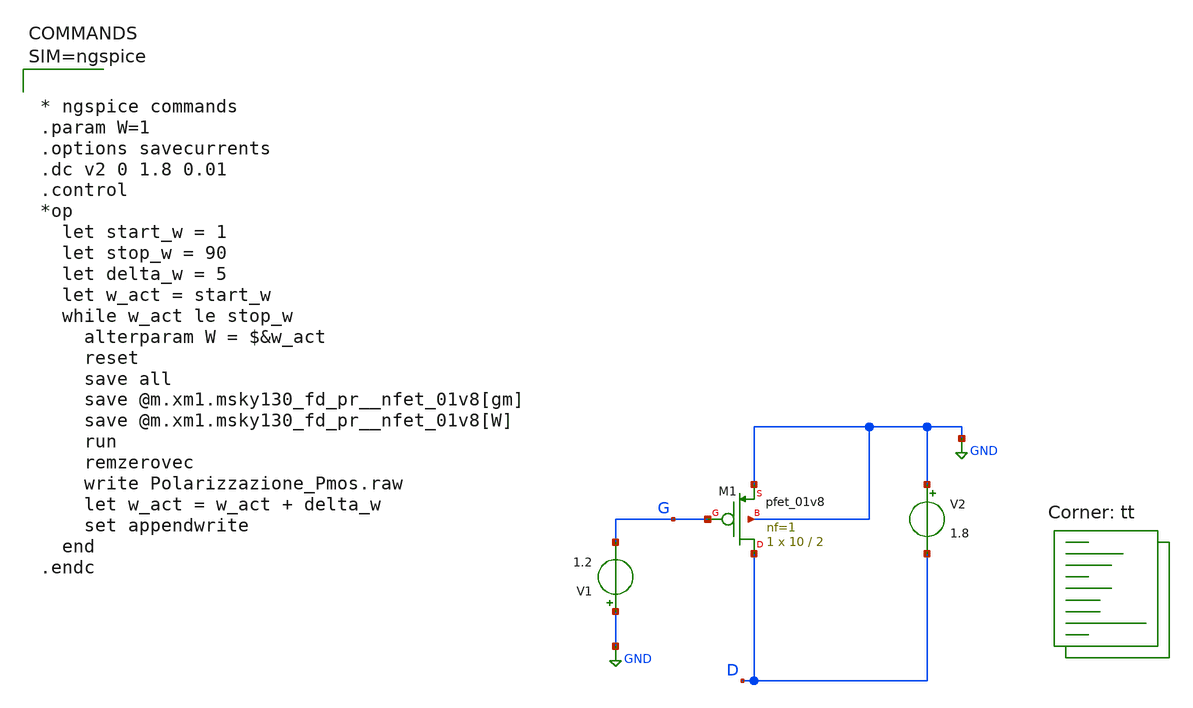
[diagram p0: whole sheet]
** sch_path: xschem/Polarizzazione_Pmos.sch
* Copyright 2021 Stefan Frederik Schippers
* Licensed under the Apache License, Version 2.0 (the "License");
* you may not use this file except in compliance with the License.
* You may obtain a copy of the License at
* https://www.apache.org/licenses/LICENSE-2.0
* Unless required by applicable law or agreed to in writing, software
* distributed under the License is distributed on an "AS IS" BASIS,
* WITHOUT WARRANTIES OR CONDITIONS OF ANY KIND, either express or implied.
* See the License for the specific language governing permissions and
* limitations under the License.
**.subckt Polarizzazione_Pmos
V1 GND G 1.2
V2 GND D 1.8
XM1 D G GND GND sky130_fd_pr__pfet_01v8 L=2 W=10 nf=1 ad='int((nf+1)/2) * W/nf * 0.29' as='int((nf+2)/2) * W/nf * 0.29'
+ pd='2*int((nf+1)/2) * (W/nf + 0.29)' ps='2*int((nf+2)/2) * (W/nf + 0.29)' nrd='0.29 / W' nrs='0.29 / W'
+ sa=0 sb=0 sd=0 mult=1 m=1
**** begin user architecture code
.lib $::SKYWATER_MODELS/sky130.lib.spice tt



* ngspice commands
.param W=1
.options savecurrents
.dc v2 0 1.8 0.01
.control
*op
  let start_w = 1
  let stop_w = 90
  let delta_w = 5
  let w_act = start_w
  while w_act le stop_w
    alterparam W = $&w_act
    reset
    save all
    save @m.xm1.msky130_fd_pr__nfet_01v8[gm]
    save @m.xm1.msky130_fd_pr__nfet_01v8[W]
    run
    remzerovec
    write Polarizzazione_Pmos.raw
    let w_act = w_act + delta_w
    set appendwrite
  end
.endc



**** end user architecture code
**.ends
.GLOBAL GND
.end
